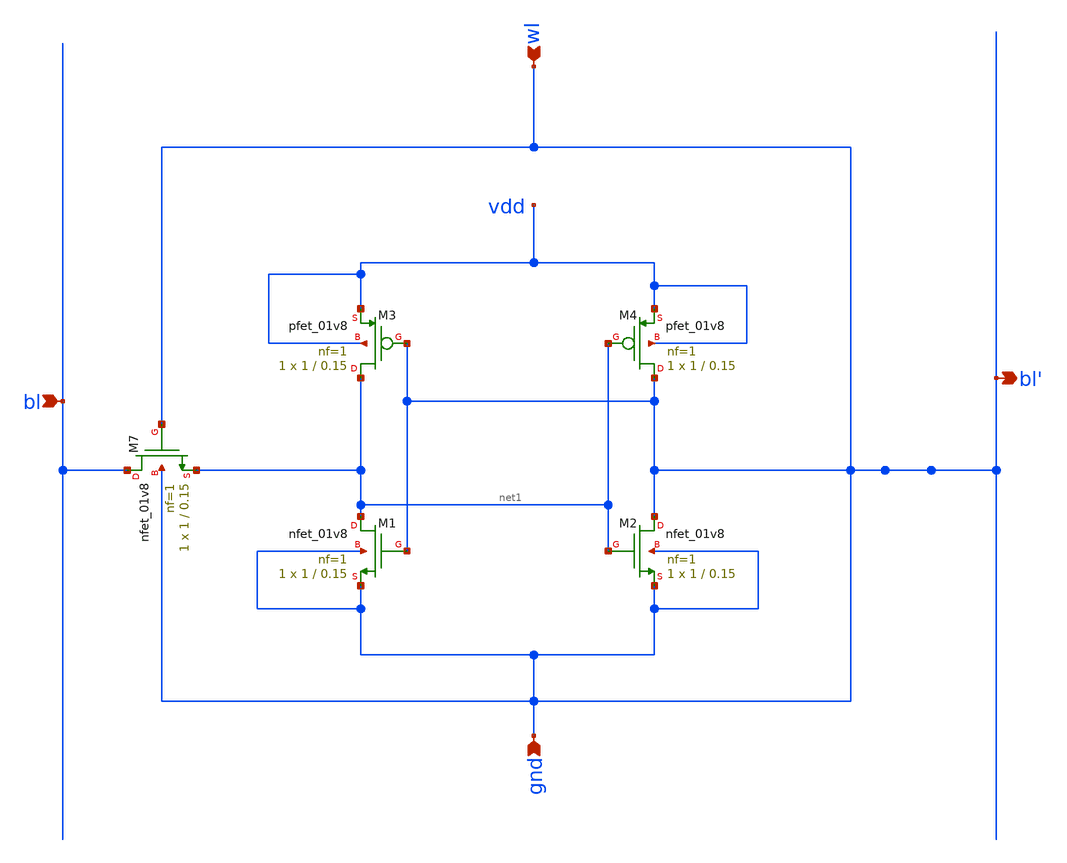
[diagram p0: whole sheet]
** sch_path: sram.sch
**.subckt sram gnd wl bl bl'
*.ipin gnd
*.ipin wl
*.ipin bl
*.opin bl'
XM1 net1 gnd gnd gnd sky130_fd_pr__nfet_01v8 L=0.15 W=1 nf=1 ad='int((nf+1)/2) * W/nf * 0.29' as='int((nf+2)/2) * W/nf * 0.29'
+ pd='2*int((nf+1)/2) * (W/nf + 0.29)' ps='2*int((nf+2)/2) * (W/nf + 0.29)' nrd='0.29 / W' nrs='0.29 / W'
+ sa=0 sb=0 sd=0 mult=1 m=1
XM2 gnd net1 gnd gnd sky130_fd_pr__nfet_01v8 L=0.15 W=1 nf=1 ad='int((nf+1)/2) * W/nf * 0.29' as='int((nf+2)/2) * W/nf * 0.29'
+ pd='2*int((nf+1)/2) * (W/nf + 0.29)' ps='2*int((nf+2)/2) * (W/nf + 0.29)' nrd='0.29 / W' nrs='0.29 / W'
+ sa=0 sb=0 sd=0 mult=1 m=1
XM3 net1 gnd vdd vdd sky130_fd_pr__pfet_01v8 L=0.15 W=1 nf=1 ad='int((nf+1)/2) * W/nf * 0.29' as='int((nf+2)/2) * W/nf * 0.29'
+ pd='2*int((nf+1)/2) * (W/nf + 0.29)' ps='2*int((nf+2)/2) * (W/nf + 0.29)' nrd='0.29 / W' nrs='0.29 / W'
+ sa=0 sb=0 sd=0 mult=1 m=1
XM4 gnd net1 vdd vdd sky130_fd_pr__pfet_01v8 L=0.15 W=1 nf=1 ad='int((nf+1)/2) * W/nf * 0.29' as='int((nf+2)/2) * W/nf * 0.29'
+ pd='2*int((nf+1)/2) * (W/nf + 0.29)' ps='2*int((nf+2)/2) * (W/nf + 0.29)' nrd='0.29 / W' nrs='0.29 / W'
+ sa=0 sb=0 sd=0 mult=1 m=1
XM7 bl gnd net1 gnd sky130_fd_pr__nfet_01v8 L=0.15 W=1 nf=1 ad='int((nf+1)/2) * W/nf * 0.29' as='int((nf+2)/2) * W/nf * 0.29'
+ pd='2*int((nf+1)/2) * (W/nf + 0.29)' ps='2*int((nf+2)/2) * (W/nf + 0.29)' nrd='0.29 / W' nrs='0.29 / W'
+ sa=0 sb=0 sd=0 mult=1 m=1
**.ends
.end
